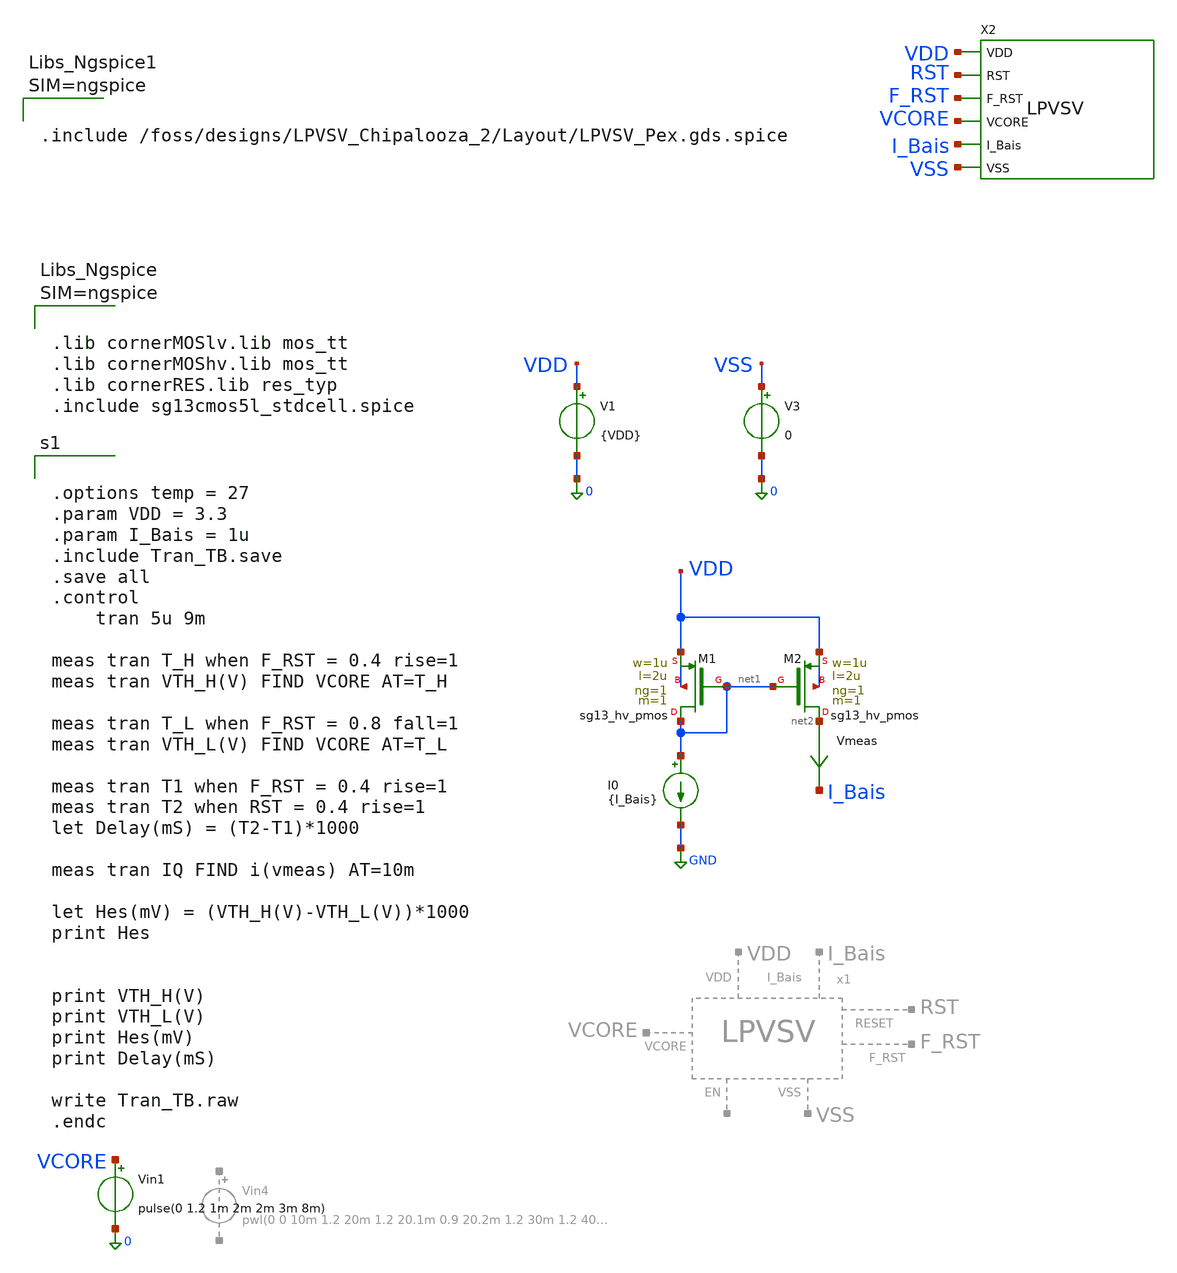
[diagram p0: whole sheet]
** sch_path: Simulation/Tran_TB.sch
**.subckt Tran_TB
I0 net1 GND {I_Bais}
V1 VDD 0 {VDD}
V3 VSS 0 0
Vin1 VCORE 0 pulse(0 1.2 1m 2m 2m 3m 8m)
Vmeas net2 I_Bais 0
.save i(vmeas)
X2 VSS F_RST VDD VCORE I_Bais RST LPVSV
XM1 net1 net1 VDD VDD sg13_hv_pmos w=1u l=2u ng=1 m=1 mm_ok=1
XM2 net2 net1 VDD VDD sg13_hv_pmos w=1u l=2u ng=1 m=1 mm_ok=1
**** begin user architecture code



.lib cornerMOSlv.lib mos_tt
.lib cornerMOShv.lib mos_tt
.lib cornerRES.lib res_typ
.include sg13cmos5l_stdcell.spice





.options temp = 27
.param VDD = 3.3
.param I_Bais = 1u
.include Tran_TB.save
.save all
.control
	tran 5u 9m

meas tran T_H when F_RST = 0.4 rise=1
meas tran VTH_H(V) FIND VCORE AT=T_H

meas tran T_L when F_RST = 0.8 fall=1
meas tran VTH_L(V) FIND VCORE AT=T_L

meas tran T1 when F_RST = 0.4 rise=1
meas tran T2 when RST = 0.4 rise=1
let Delay(mS) = (T2-T1)*1000

meas tran IQ FIND i(vmeas) AT=10m

let Hes(mV) = (VTH_H(V)-VTH_L(V))*1000
print Hes


print VTH_H(V)
print VTH_L(V)
print Hes(mV)
print Delay(mS)

write Tran_TB.raw
.endc





.include /foss/designs/LPVSV_Chipalooza_2/Layout/LPVSV_Pex.gds.spice



**** end user architecture code
**.ends
.GLOBAL GND
.end
